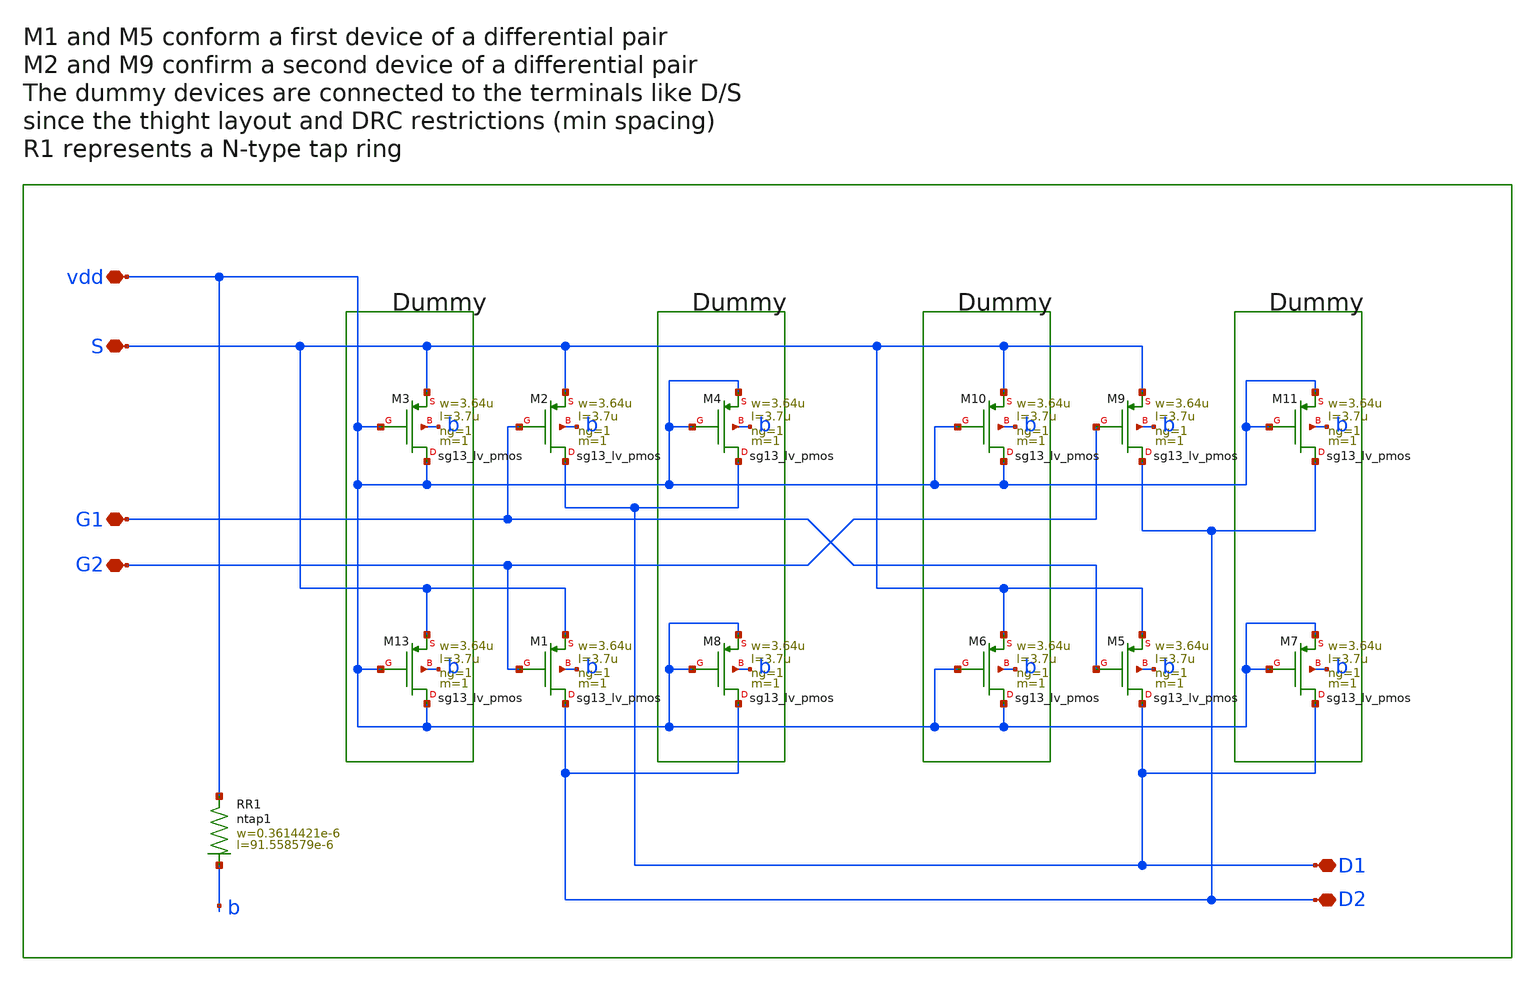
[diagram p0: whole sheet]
** sch_path: OTA1336-main/schematic/xschem/diff_pair.sch
**.subckt diff_pair D1 D2 vdd S G1 G2
*.iopin D1
*.iopin D2
*.iopin vdd
*.iopin S
*.iopin G1
*.iopin G2
XM1 D2 G2 S b sg13_lv_pmos w=3.64u l=3.7u ng=1 m=1 mm_ok=1
XM13 vdd vdd S b sg13_lv_pmos w=3.64u l=3.7u ng=1 m=1 mm_ok=1
XR1 vdd b ntap1 R=4.518 w=0.3614421e-6 l=91.558579e-6
XM8 D2 vdd vdd b sg13_lv_pmos w=3.64u l=3.7u ng=1 m=1 mm_ok=1
XM2 D1 G1 S b sg13_lv_pmos w=3.64u l=3.7u ng=1 m=1 mm_ok=1
XM3 vdd vdd S b sg13_lv_pmos w=3.64u l=3.7u ng=1 m=1 mm_ok=1
XM4 D1 vdd vdd b sg13_lv_pmos w=3.64u l=3.7u ng=1 m=1 mm_ok=1
XM5 D1 G1 S b sg13_lv_pmos w=3.64u l=3.7u ng=1 m=1 mm_ok=1
XM6 vdd vdd S b sg13_lv_pmos w=3.64u l=3.7u ng=1 m=1 mm_ok=1
XM7 D1 vdd vdd b sg13_lv_pmos w=3.64u l=3.7u ng=1 m=1 mm_ok=1
XM9 D2 G2 S b sg13_lv_pmos w=3.64u l=3.7u ng=1 m=1 mm_ok=1
XM10 vdd vdd S b sg13_lv_pmos w=3.64u l=3.7u ng=1 m=1 mm_ok=1
XM11 D2 vdd vdd b sg13_lv_pmos w=3.64u l=3.7u ng=1 m=1 mm_ok=1
**.ends
.end
